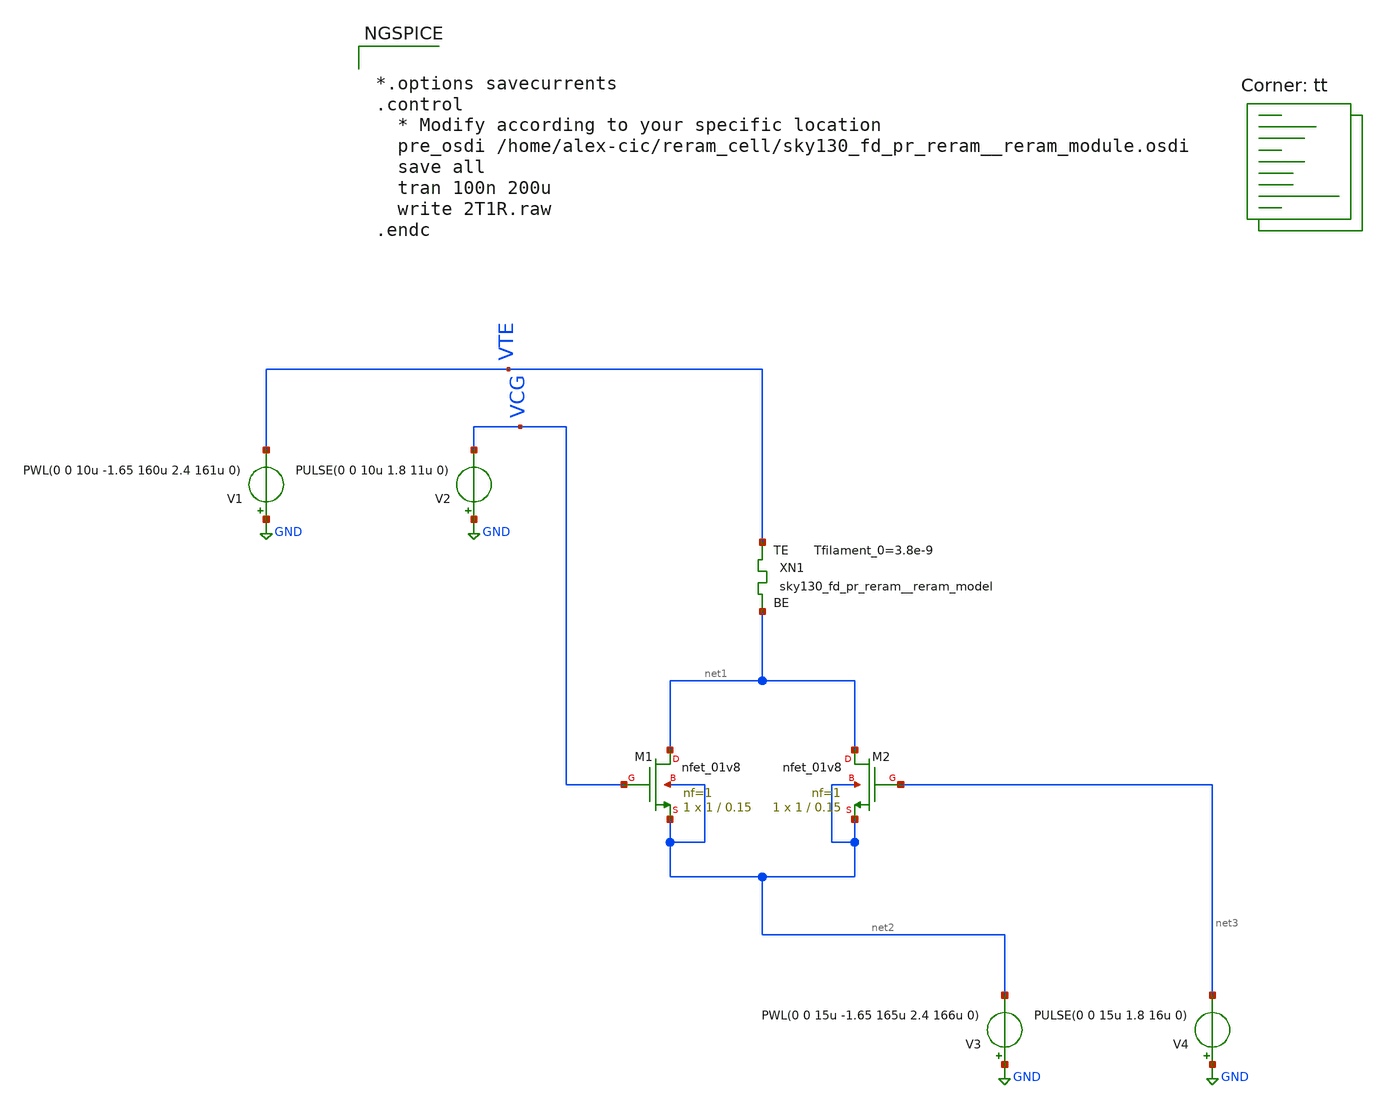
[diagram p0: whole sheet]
** sch_path: Synapse/2T1R.sch
* StefanSchippers/xschem_sky130/sky130_fd_pr/reram.sym:
* Copyright 2021 Stefan Frederik Schippers
* Licensed under the Apache License, Version 2.0 (the "License");
**.subckt 2T1R
XN1 VTE net1 sky130_fd_pr_reram__reram_model Tfilament_0=3.8e-9
XM1 net1 VCG net2 net2 sky130_fd_pr__nfet_01v8 L=0.15 W=1 nf=1 ad='int((nf+1)/2) * W/nf * 0.29' as='int((nf+2)/2) * W/nf * 0.29'
+ pd='2*int((nf+1)/2) * (W/nf + 0.29)' ps='2*int((nf+2)/2) * (W/nf + 0.29)' nrd='0.29 / W' nrs='0.29 / W'
+ sa=0 sb=0 sd=0 mult=1 m=1
XM2 net1 net3 net2 net2 sky130_fd_pr__nfet_01v8 L=0.15 W=1 nf=1 ad='int((nf+1)/2) * W/nf * 0.29' as='int((nf+2)/2) * W/nf * 0.29'
+ pd='2*int((nf+1)/2) * (W/nf + 0.29)' ps='2*int((nf+2)/2) * (W/nf + 0.29)' nrd='0.29 / W' nrs='0.29 / W'
+ sa=0 sb=0 sd=0 mult=1 m=1
V1 GND VTE
PWL(0 0 10u -1.65 160u 2.4 161u 0)

V2 GND VCG PULSE(0 0 10u 1.8 11u 0)
V3 GND net2
PWL(0 0 15u -1.65 165u 2.4 166u 0)

V4 GND net3 PULSE(0 0 15u 1.8 16u 0)
**** begin user architecture code
.lib $::SKYWATER_MODELS/sky130.lib.spice tt


*.options savecurrents
.control
  * Modify according to your specific location
  pre_osdi /home/alex-cic/reram_cell/sky130_fd_pr_reram__reram_module.osdi
  save all
  tran 100n 200u
  write 2T1R.raw
.endc



**** end user architecture code
**.ends
.GLOBAL GND
**** begin user architecture code

.subckt sky130_fd_pr_reram__reram_cell TE BE Tfilament_0=3.3e-9 area_ox=0.1024e-12
N1 TE BE nFilament sky130_fd_pr_reram__reram_model
.ic v(nFilament)={Tfilament_0*1.0e9}
.ends sky130_fd_pr_reram__reram_cell

.model sky130_fd_pr_reram__reram_model sky130_fd_pr_reram__reram_module  area_ox = 0.1024e-12  Tox =
+ 5.0  Tfilament_max = 4.9  Tfilament_min = 3.3  Eact_generation = 1.501  Eact_recombination  = 1.500
+  I_k1  = 6.140e-5  Tfilament_ref = 4.7249  V_ref = 0.430  velocity_k1 = 150  gamma_k0  = 16.5  gamma_k1
+  = -1.25  Temperature_0 = 300  C_thermal = 3.1825e-16  tau_thermal = 0.23e-9  t_step  = 1.0e-9
+  smoothing = 1e-7  Kclip = 200

.control
pre_osdi $SKYWATER_MODELS/sky130_fd_pr_reram__reram_module.osdi
.endc

**** end user architecture code
.end
